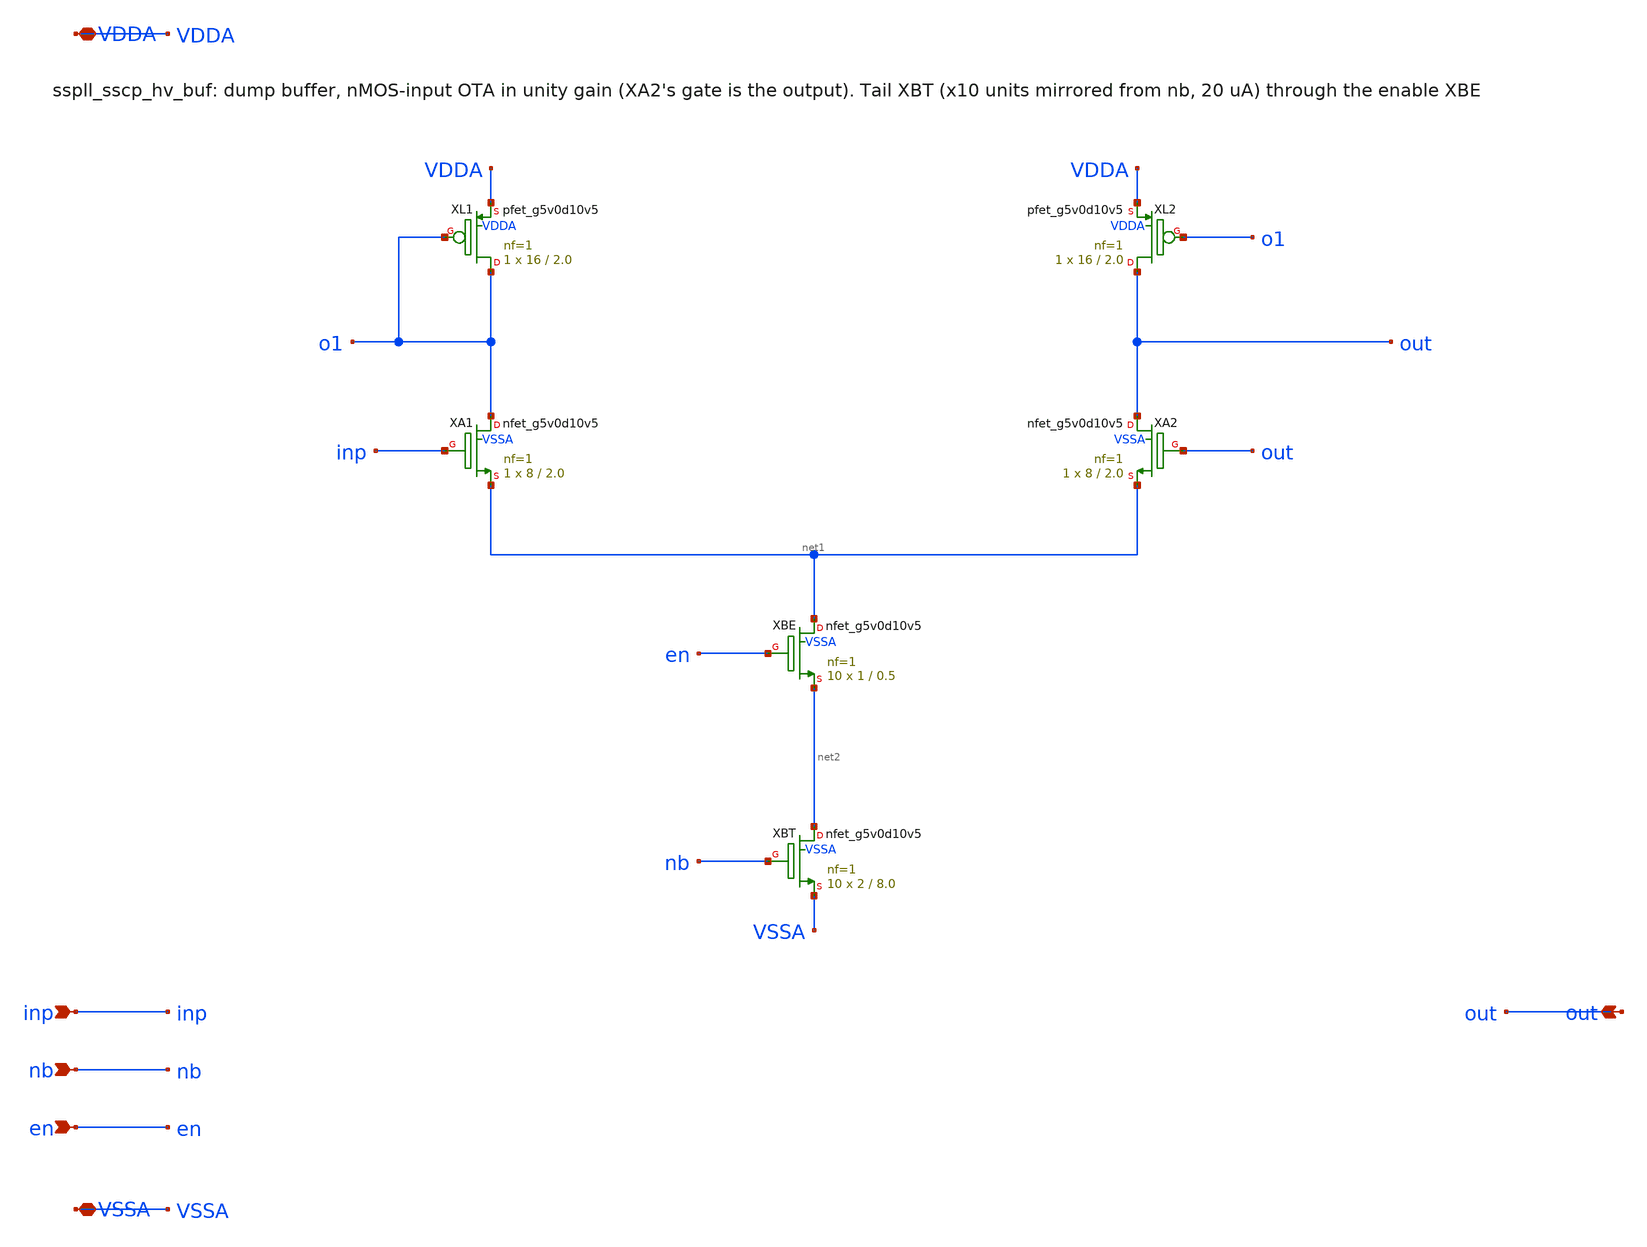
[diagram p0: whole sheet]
** sch_path: xschem/sscp_hv/sspll_sscp_hv_buf.sch
**.subckt sspll_sscp_hv_buf inp nb en out VDDA VSSA
*.ipin inp
*.ipin nb
*.ipin en
*.opin out
*.iopin VDDA
*.iopin VSSA
XXL1 o1 o1 VDDA VDDA sky130_fd_pr__pfet_g5v0d10v5 L=2.0 W=16 nf=1 ad='int((nf+1)/2) * W/nf * 0.29' as='int((nf+2)/2) * W/nf * 0.29'
+ pd='2*int((nf+1)/2) * (W/nf + 0.29)' ps='2*int((nf+2)/2) * (W/nf + 0.29)' nrd='0.29 / W' nrs='0.29 / W'
+ sa=0 sb=0 sd=0 mult=1 m=1
XXL2 out o1 VDDA VDDA sky130_fd_pr__pfet_g5v0d10v5 L=2.0 W=16 nf=1 ad='int((nf+1)/2) * W/nf * 0.29' as='int((nf+2)/2) * W/nf * 0.29'
+ pd='2*int((nf+1)/2) * (W/nf + 0.29)' ps='2*int((nf+2)/2) * (W/nf + 0.29)' nrd='0.29 / W' nrs='0.29 / W'
+ sa=0 sb=0 sd=0 mult=1 m=1
XXA1 o1 inp net1 VSSA sky130_fd_pr__nfet_g5v0d10v5 L=2.0 W=8 nf=1 ad='int((nf+1)/2) * W/nf * 0.29' as='int((nf+2)/2) * W/nf * 0.29'
+ pd='2*int((nf+1)/2) * (W/nf + 0.29)' ps='2*int((nf+2)/2) * (W/nf + 0.29)' nrd='0.29 / W' nrs='0.29 / W'
+ sa=0 sb=0 sd=0 mult=1 m=1
XXA2 out out net1 VSSA sky130_fd_pr__nfet_g5v0d10v5 L=2.0 W=8 nf=1 ad='int((nf+1)/2) * W/nf * 0.29' as='int((nf+2)/2) * W/nf * 0.29'
+ pd='2*int((nf+1)/2) * (W/nf + 0.29)' ps='2*int((nf+2)/2) * (W/nf + 0.29)' nrd='0.29 / W' nrs='0.29 / W'
+ sa=0 sb=0 sd=0 mult=1 m=1
XXBE net1 en net2 VSSA sky130_fd_pr__nfet_g5v0d10v5 L=0.5 W=1 nf=1 ad='int((nf+1)/2) * W/nf * 0.29' as='int((nf+2)/2) * W/nf * 0.29'
+ pd='2*int((nf+1)/2) * (W/nf + 0.29)' ps='2*int((nf+2)/2) * (W/nf + 0.29)' nrd='0.29 / W' nrs='0.29 / W'
+ sa=0 sb=0 sd=0 mult=10 m=10
XXBT net2 nb VSSA VSSA sky130_fd_pr__nfet_g5v0d10v5 L=8.0 W=2 nf=1 ad='int((nf+1)/2) * W/nf * 0.29' as='int((nf+2)/2) * W/nf * 0.29'
+ pd='2*int((nf+1)/2) * (W/nf + 0.29)' ps='2*int((nf+2)/2) * (W/nf + 0.29)' nrd='0.29 / W' nrs='0.29 / W'
+ sa=0 sb=0 sd=0 mult=10 m=10
**.ends
.end
